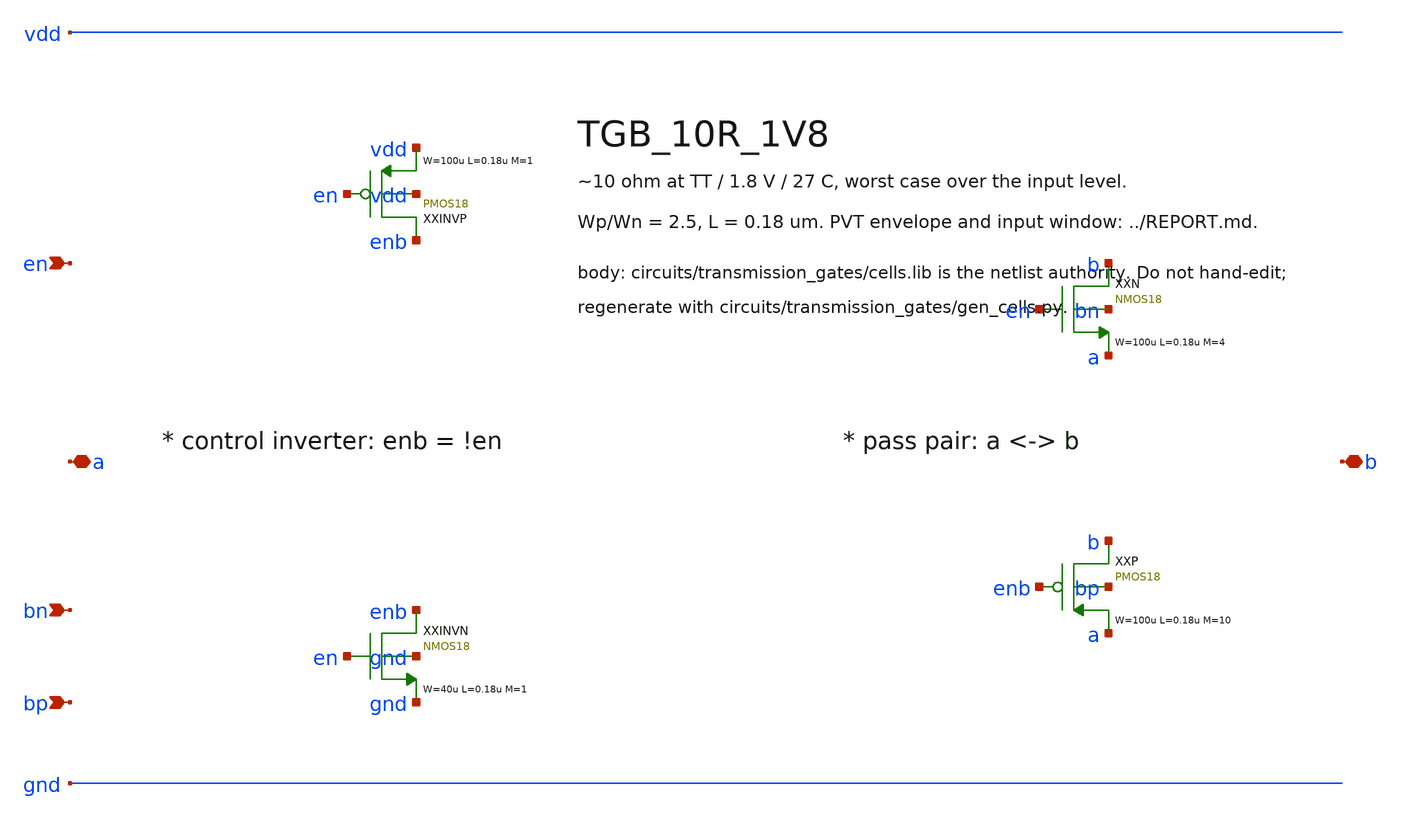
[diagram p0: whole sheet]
** sch_path: xschem/transmission_gates/TGB_10R_1V8.sch
**.subckt TGB_10R_1V8 a b en bn bp
*.iopin a
*.iopin b
*.ipin en
*.ipin bn
*.ipin bp
XXINVP enb en vdd vdd PMOS18 W=100u L=0.18u M=1 MM_SIGMA=0
XXINVN enb en gnd gnd NMOS18 W=40u L=0.18u M=1 MM_SIGMA=0
XXN b en a bn NMOS18 W=100u L=0.18u M=4 MM_SIGMA=0
XXP b enb a bp PMOS18 W=100u L=0.18u M=10 MM_SIGMA=0
**.ends
.end
